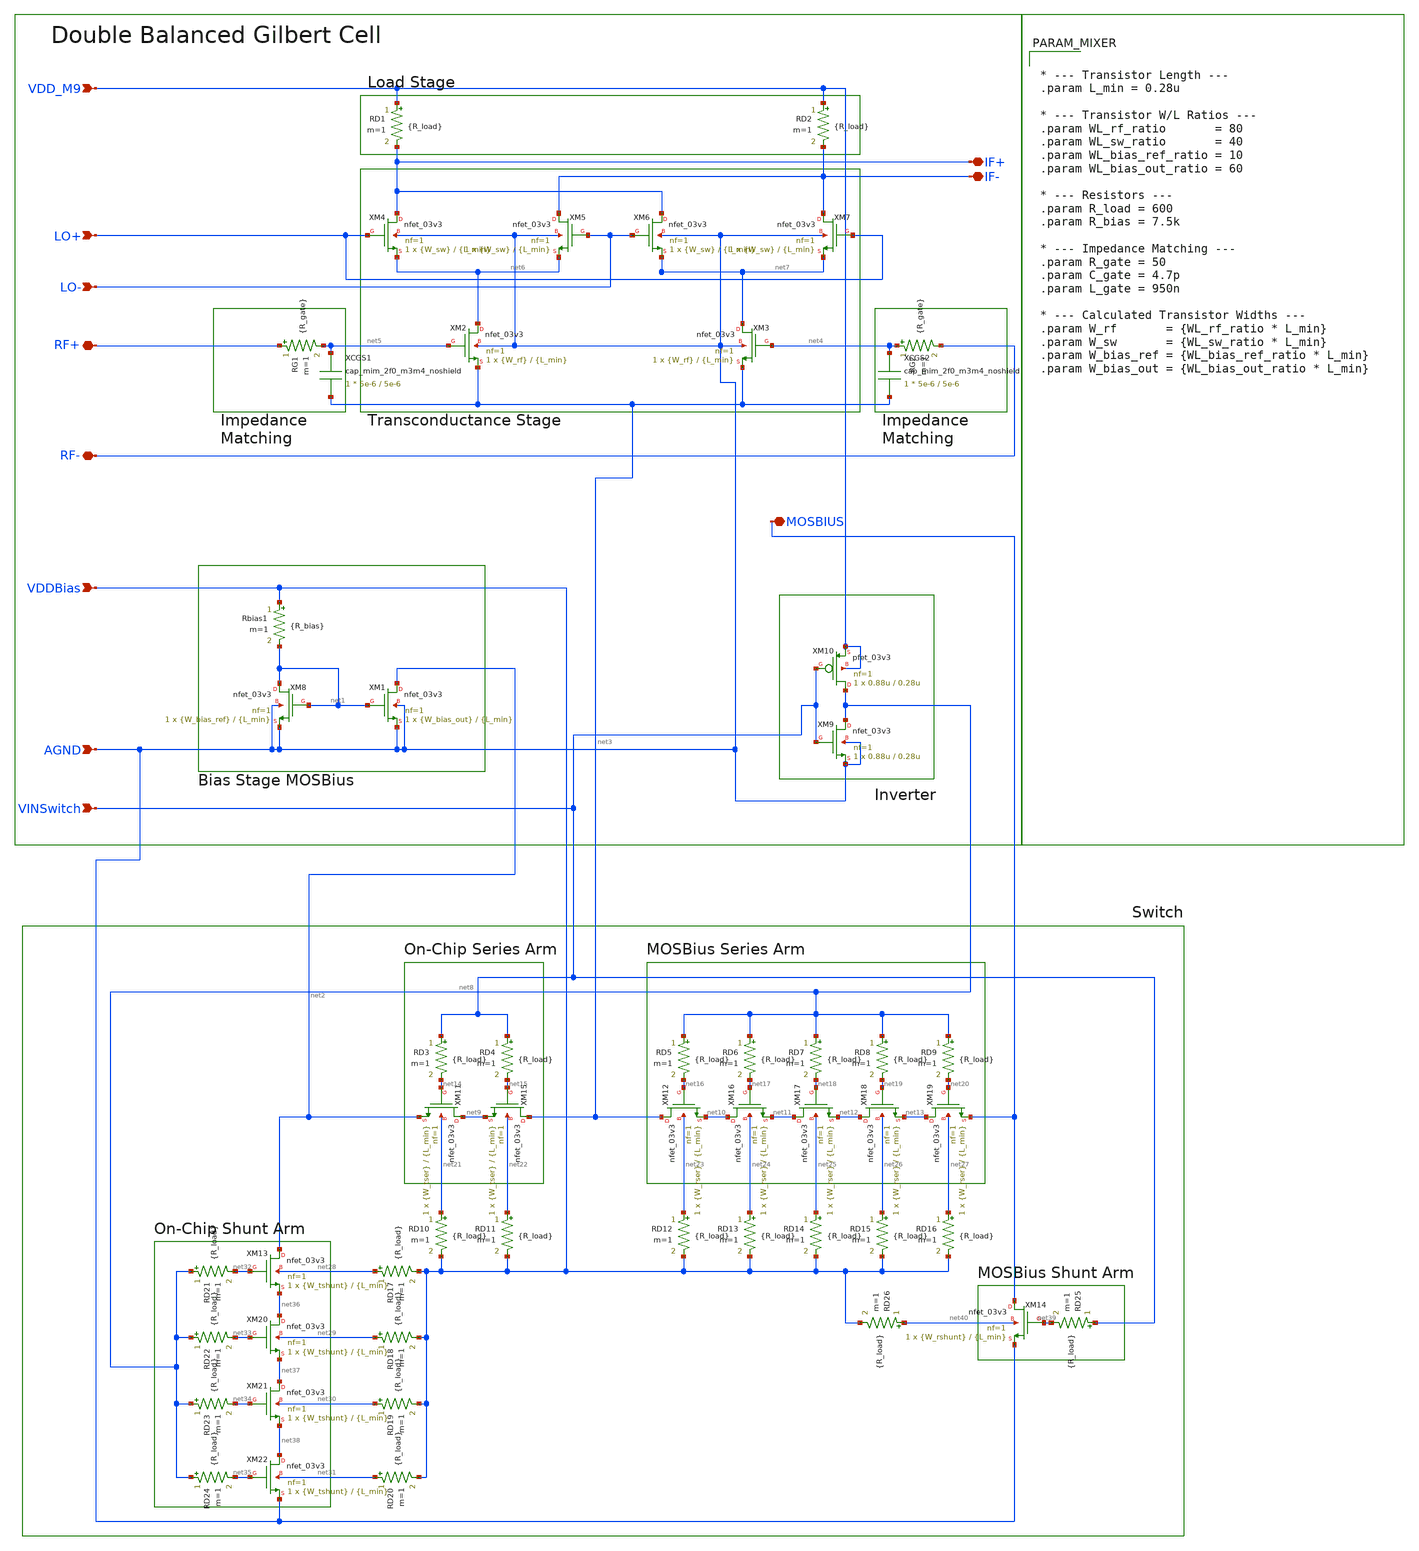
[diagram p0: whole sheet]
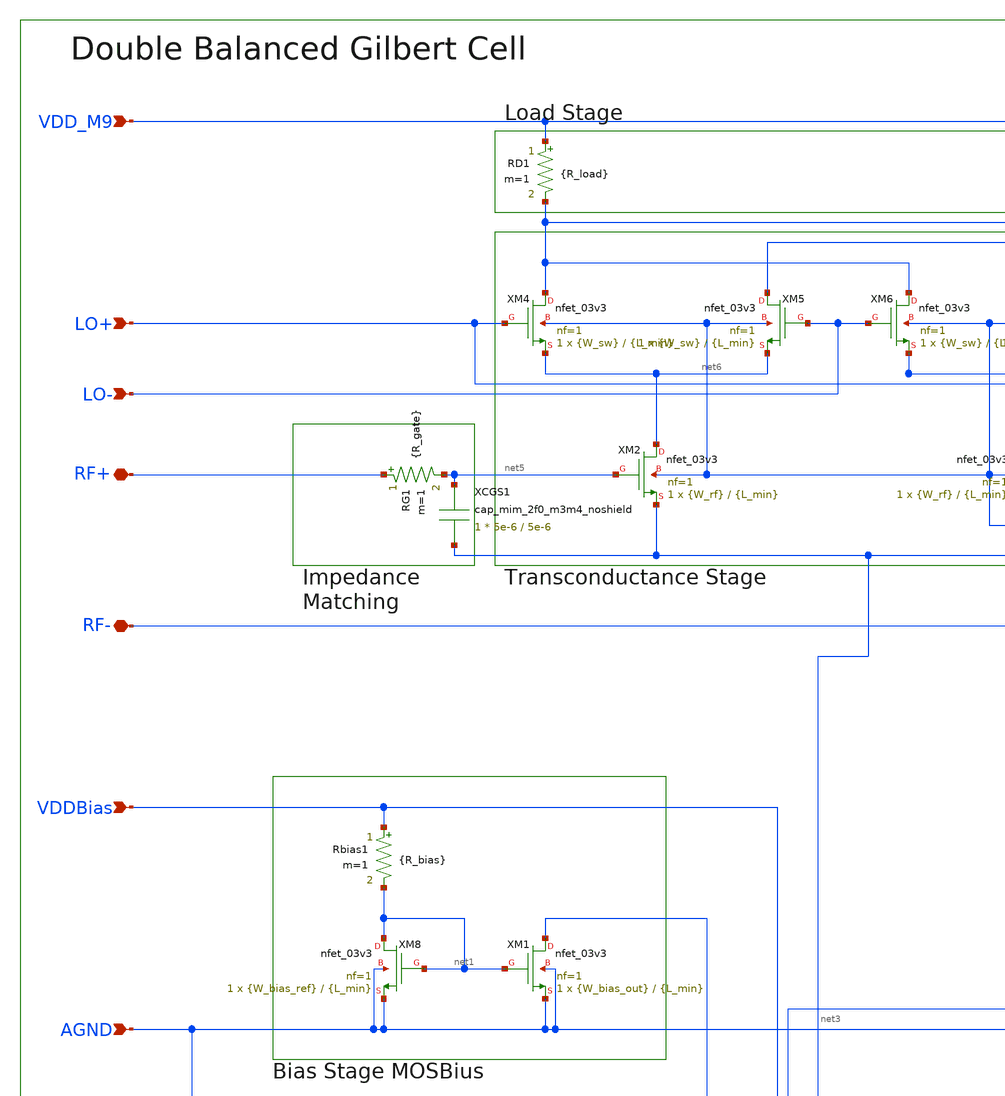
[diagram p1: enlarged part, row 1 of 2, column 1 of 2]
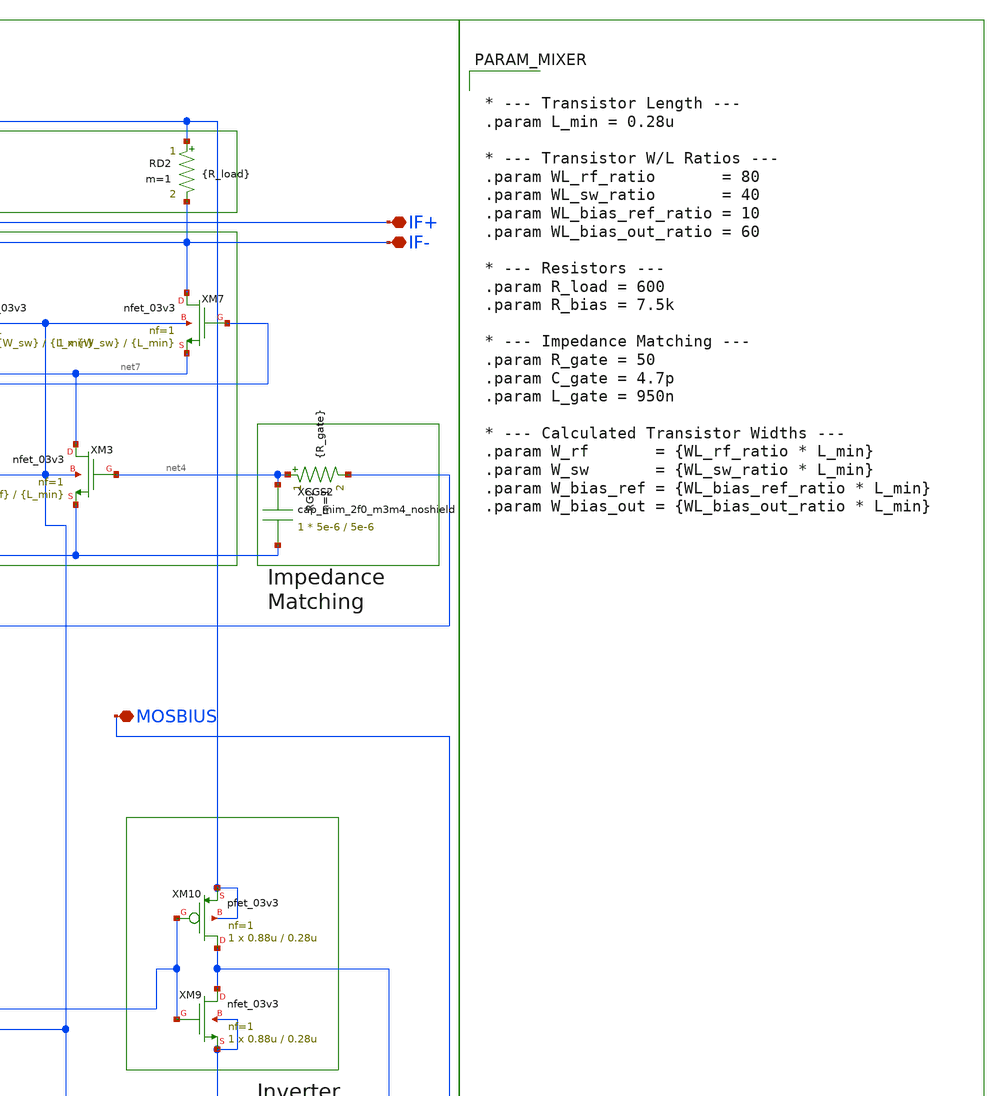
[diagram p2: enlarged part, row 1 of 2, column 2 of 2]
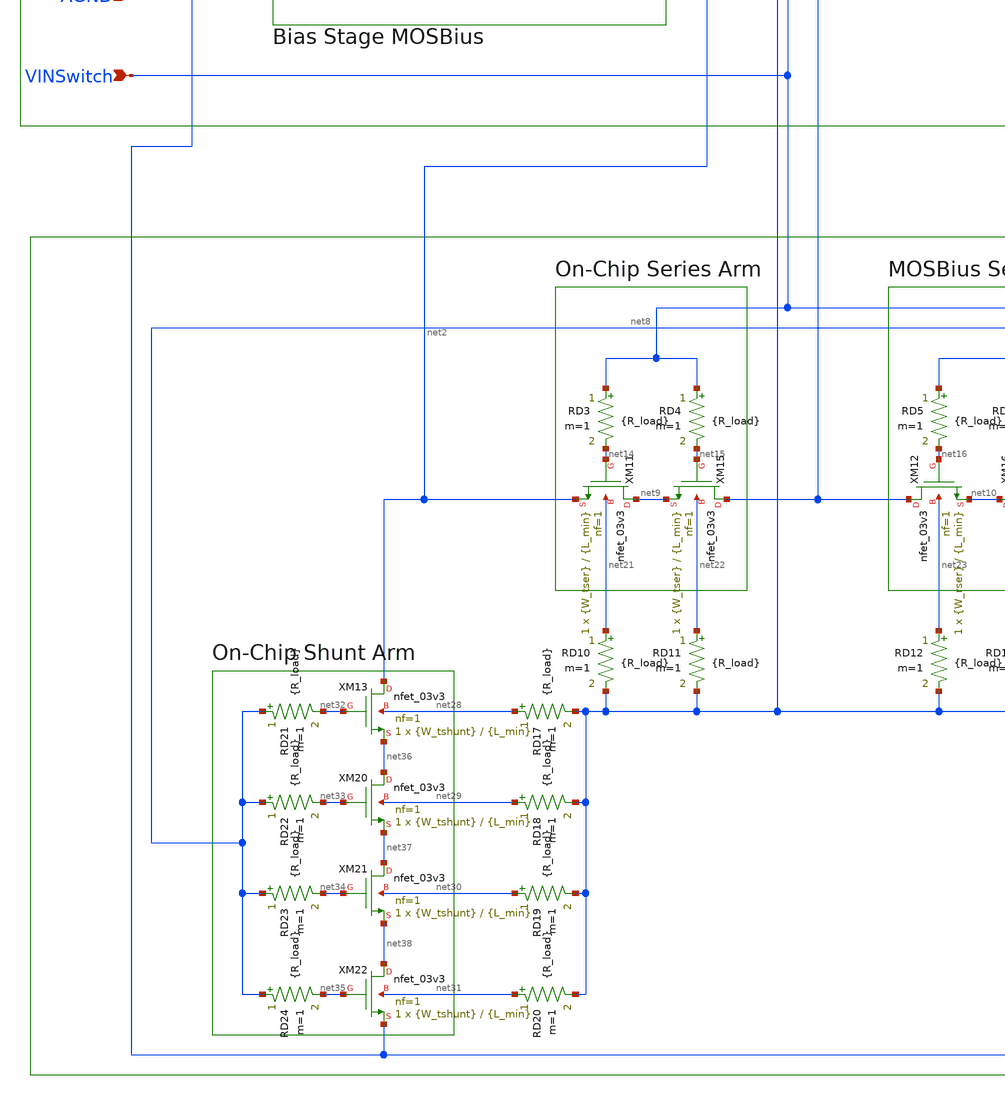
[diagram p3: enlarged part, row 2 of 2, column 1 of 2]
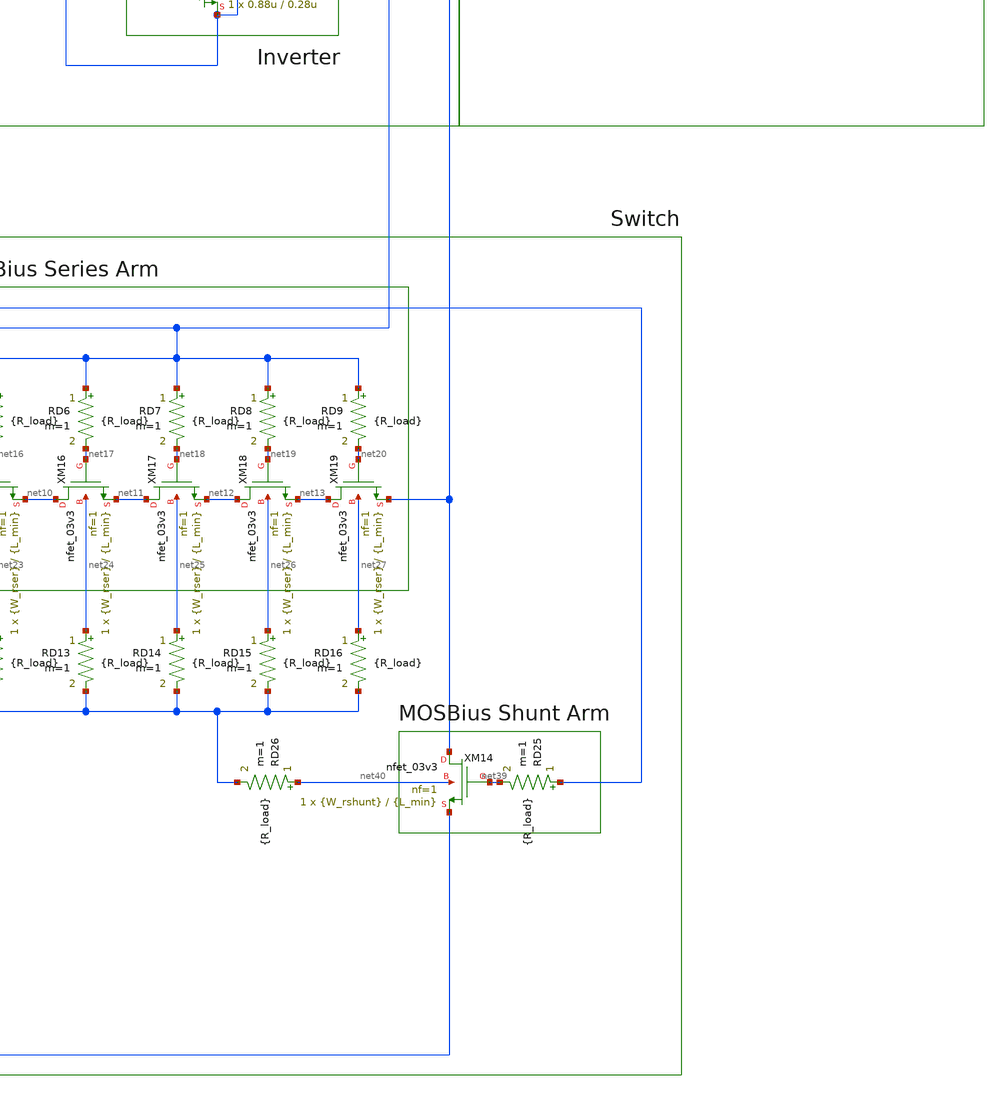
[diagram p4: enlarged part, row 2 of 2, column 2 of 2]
** sch_path: designs/libs/LVS/ReconfigMixer.sch
**.subckt ReconfigMixer AGND RF- IF+ VDD_M9 LO+ LO- IF- RF+ VDDBias MOSBIUS VINSwitch
*.ipin AGND
*.iopin RF-
*.iopin IF+
*.ipin VDD_M9
*.ipin LO+
*.ipin LO-
*.iopin IF-
*.iopin RF+
*.ipin VDDBias
*.iopin MOSBIUS
*.ipin VINSwitch
XM8 net1 net1 AGND AGND nfet_03v3 L={L_min} W={W_bias_ref} nf=1 ad='int((nf+1)/2) * W/nf * 0.18u' as='int((nf+2)/2) * W/nf * 0.18u'
+ pd='2*int((nf+1)/2) * (W/nf + 0.18u)' ps='2*int((nf+2)/2) * (W/nf + 0.18u)' nrd='0.18u / W' nrs='0.18u / W'
+ sa=0 sb=0 sd=0 m=1
XM1 net2 net1 AGND AGND nfet_03v3 L={L_min} W={W_bias_out} nf=1 ad='int((nf+1)/2) * W/nf * 0.18u' as='int((nf+2)/2) * W/nf * 0.18u'
+ pd='2*int((nf+1)/2) * (W/nf + 0.18u)' ps='2*int((nf+2)/2) * (W/nf + 0.18u)' nrd='0.18u / W' nrs='0.18u / W'
+ sa=0 sb=0 sd=0 m=1
XM3 net7 net4 net3 AGND nfet_03v3 L={L_min} W={W_rf} nf=1 ad='int((nf+1)/2) * W/nf * 0.18u' as='int((nf+2)/2) * W/nf * 0.18u'
+ pd='2*int((nf+1)/2) * (W/nf + 0.18u)' ps='2*int((nf+2)/2) * (W/nf + 0.18u)' nrd='0.18u / W' nrs='0.18u / W'
+ sa=0 sb=0 sd=0 m=1
XM2 net6 net5 net3 AGND nfet_03v3 L={L_min} W={W_rf} nf=1 ad='int((nf+1)/2) * W/nf * 0.18u' as='int((nf+2)/2) * W/nf * 0.18u'
+ pd='2*int((nf+1)/2) * (W/nf + 0.18u)' ps='2*int((nf+2)/2) * (W/nf + 0.18u)' nrd='0.18u / W' nrs='0.18u / W'
+ sa=0 sb=0 sd=0 m=1
XM7 IF- LO+ net7 AGND nfet_03v3 L={L_min} W={W_sw} nf=1 ad='int((nf+1)/2) * W/nf * 0.18u' as='int((nf+2)/2) * W/nf * 0.18u'
+ pd='2*int((nf+1)/2) * (W/nf + 0.18u)' ps='2*int((nf+2)/2) * (W/nf + 0.18u)' nrd='0.18u / W' nrs='0.18u / W'
+ sa=0 sb=0 sd=0 m=1
XM6 IF+ LO- net7 AGND nfet_03v3 L={L_min} W={W_sw} nf=1 ad='int((nf+1)/2) * W/nf * 0.18u' as='int((nf+2)/2) * W/nf * 0.18u'
+ pd='2*int((nf+1)/2) * (W/nf + 0.18u)' ps='2*int((nf+2)/2) * (W/nf + 0.18u)' nrd='0.18u / W' nrs='0.18u / W'
+ sa=0 sb=0 sd=0 m=1
XM5 IF- LO- net6 AGND nfet_03v3 L={L_min} W={W_sw} nf=1 ad='int((nf+1)/2) * W/nf * 0.18u' as='int((nf+2)/2) * W/nf * 0.18u'
+ pd='2*int((nf+1)/2) * (W/nf + 0.18u)' ps='2*int((nf+2)/2) * (W/nf + 0.18u)' nrd='0.18u / W' nrs='0.18u / W'
+ sa=0 sb=0 sd=0 m=1
XM4 IF+ LO+ net6 AGND nfet_03v3 L={L_min} W={W_sw} nf=1 ad='int((nf+1)/2) * W/nf * 0.18u' as='int((nf+2)/2) * W/nf * 0.18u'
+ pd='2*int((nf+1)/2) * (W/nf + 0.18u)' ps='2*int((nf+2)/2) * (W/nf + 0.18u)' nrd='0.18u / W' nrs='0.18u / W'
+ sa=0 sb=0 sd=0 m=1
RD1 VDD_M9 IF+ {R_load} m=1
RD2 VDD_M9 IF- {R_load} m=1
RG1 RF+ net5 {R_gate} m=1
RG2 net4 RF- {R_gate} m=1
Rbias1 VDDBias net1 {R_bias} m=1
XCGS2 net4 net3 cap_mim_2f0_m3m4_noshield c_width=5e-6 c_length=5e-6 m=1
XCGS1 net5 net3 cap_mim_2f0_m3m4_noshield c_width=5e-6 c_length=5e-6 m=1
XM9 net8 VINSwitch AGND AGND nfet_03v3 L=0.28u W=0.88u nf=1 ad='int((nf+1)/2) * W/nf * 0.18u' as='int((nf+2)/2) * W/nf * 0.18u'
+ pd='2*int((nf+1)/2) * (W/nf + 0.18u)' ps='2*int((nf+2)/2) * (W/nf + 0.18u)' nrd='0.18u / W' nrs='0.18u / W'
+ sa=0 sb=0 sd=0 m=1
XM10 net8 VINSwitch VDD_M9 VDD_M9 pfet_03v3 L=0.28u W=0.88u nf=1 ad='int((nf+1)/2) * W/nf * 0.18u' as='int((nf+2)/2) * W/nf * 0.18u'
+ pd='2*int((nf+1)/2) * (W/nf + 0.18u)' ps='2*int((nf+2)/2) * (W/nf + 0.18u)' nrd='0.18u / W' nrs='0.18u / W'
+ sa=0 sb=0 sd=0 m=1
XM11 net9 net14 net2 net21 nfet_03v3 L={L_min} W={W_tser} nf=1 ad='int((nf+1)/2) * W/nf * 0.18u' as='int((nf+2)/2) * W/nf * 0.18u'
+ pd='2*int((nf+1)/2) * (W/nf + 0.18u)' ps='2*int((nf+2)/2) * (W/nf + 0.18u)' nrd='0.18u / W' nrs='0.18u / W'
+ sa=0 sb=0 sd=0 m=1
XM12 net3 net16 net10 net23 nfet_03v3 L={L_min} W={W_rser} nf=1 ad='int((nf+1)/2) * W/nf * 0.18u' as='int((nf+2)/2) * W/nf * 0.18u'
+ pd='2*int((nf+1)/2) * (W/nf + 0.18u)' ps='2*int((nf+2)/2) * (W/nf + 0.18u)' nrd='0.18u / W' nrs='0.18u / W'
+ sa=0 sb=0 sd=0 m=1
XM13 net2 net32 net36 net28 nfet_03v3 L={L_min} W={W_tshunt} nf=1 ad='int((nf+1)/2) * W/nf * 0.18u' as='int((nf+2)/2) * W/nf * 0.18u'
+ pd='2*int((nf+1)/2) * (W/nf + 0.18u)' ps='2*int((nf+2)/2) * (W/nf + 0.18u)' nrd='0.18u / W' nrs='0.18u / W'
+ sa=0 sb=0 sd=0 m=1
XM14 MOSBIUS net39 AGND net40 nfet_03v3 L={L_min} W={W_rshunt} nf=1 ad='int((nf+1)/2) * W/nf * 0.18u'
+ as='int((nf+2)/2) * W/nf * 0.18u' pd='2*int((nf+1)/2) * (W/nf + 0.18u)' ps='2*int((nf+2)/2) * (W/nf + 0.18u)'
+ nrd='0.18u / W' nrs='0.18u / W' sa=0 sb=0 sd=0 m=1
XM15 net3 net15 net9 net22 nfet_03v3 L={L_min} W={W_tser} nf=1 ad='int((nf+1)/2) * W/nf * 0.18u' as='int((nf+2)/2) * W/nf * 0.18u'
+ pd='2*int((nf+1)/2) * (W/nf + 0.18u)' ps='2*int((nf+2)/2) * (W/nf + 0.18u)' nrd='0.18u / W' nrs='0.18u / W'
+ sa=0 sb=0 sd=0 m=1
RD3 VINSwitch net14 {R_load} m=1
RD4 VINSwitch net15 {R_load} m=1
RD5 net8 net16 {R_load} m=1
RD6 net8 net17 {R_load} m=1
RD7 net8 net18 {R_load} m=1
RD8 net8 net19 {R_load} m=1
RD9 net8 net20 {R_load} m=1
RD10 net21 VDDBias {R_load} m=1
RD11 net22 VDDBias {R_load} m=1
RD12 net23 VDDBias {R_load} m=1
RD13 net24 VDDBias {R_load} m=1
RD14 net25 VDDBias {R_load} m=1
RD15 net26 VDDBias {R_load} m=1
RD16 net27 VDDBias {R_load} m=1
RD17 net28 VDDBias {R_load} m=1
RD18 net29 VDDBias {R_load} m=1
RD19 net30 VDDBias {R_load} m=1
RD20 net31 VDDBias {R_load} m=1
RD21 net8 net32 {R_load} m=1
RD22 net8 net33 {R_load} m=1
RD23 net8 net34 {R_load} m=1
RD24 net8 net35 {R_load} m=1
XM16 net10 net17 net11 net24 nfet_03v3 L={L_min} W={W_rser} nf=1 ad='int((nf+1)/2) * W/nf * 0.18u' as='int((nf+2)/2) * W/nf * 0.18u'
+ pd='2*int((nf+1)/2) * (W/nf + 0.18u)' ps='2*int((nf+2)/2) * (W/nf + 0.18u)' nrd='0.18u / W' nrs='0.18u / W'
+ sa=0 sb=0 sd=0 m=1
XM17 net11 net18 net12 net25 nfet_03v3 L={L_min} W={W_rser} nf=1 ad='int((nf+1)/2) * W/nf * 0.18u' as='int((nf+2)/2) * W/nf * 0.18u'
+ pd='2*int((nf+1)/2) * (W/nf + 0.18u)' ps='2*int((nf+2)/2) * (W/nf + 0.18u)' nrd='0.18u / W' nrs='0.18u / W'
+ sa=0 sb=0 sd=0 m=1
XM18 net12 net19 net13 net26 nfet_03v3 L={L_min} W={W_rser} nf=1 ad='int((nf+1)/2) * W/nf * 0.18u' as='int((nf+2)/2) * W/nf * 0.18u'
+ pd='2*int((nf+1)/2) * (W/nf + 0.18u)' ps='2*int((nf+2)/2) * (W/nf + 0.18u)' nrd='0.18u / W' nrs='0.18u / W'
+ sa=0 sb=0 sd=0 m=1
XM19 net13 net20 MOSBIUS net27 nfet_03v3 L={L_min} W={W_rser} nf=1 ad='int((nf+1)/2) * W/nf * 0.18u'
+ as='int((nf+2)/2) * W/nf * 0.18u' pd='2*int((nf+1)/2) * (W/nf + 0.18u)' ps='2*int((nf+2)/2) * (W/nf + 0.18u)'
+ nrd='0.18u / W' nrs='0.18u / W' sa=0 sb=0 sd=0 m=1
RD25 VINSwitch net39 {R_load} m=1
XM20 net36 net33 net37 net29 nfet_03v3 L={L_min} W={W_tshunt} nf=1 ad='int((nf+1)/2) * W/nf * 0.18u'
+ as='int((nf+2)/2) * W/nf * 0.18u' pd='2*int((nf+1)/2) * (W/nf + 0.18u)' ps='2*int((nf+2)/2) * (W/nf + 0.18u)'
+ nrd='0.18u / W' nrs='0.18u / W' sa=0 sb=0 sd=0 m=1
XM21 net37 net34 net38 net30 nfet_03v3 L={L_min} W={W_tshunt} nf=1 ad='int((nf+1)/2) * W/nf * 0.18u'
+ as='int((nf+2)/2) * W/nf * 0.18u' pd='2*int((nf+1)/2) * (W/nf + 0.18u)' ps='2*int((nf+2)/2) * (W/nf + 0.18u)'
+ nrd='0.18u / W' nrs='0.18u / W' sa=0 sb=0 sd=0 m=1
XM22 net38 net35 AGND net31 nfet_03v3 L={L_min} W={W_tshunt} nf=1 ad='int((nf+1)/2) * W/nf * 0.18u' as='int((nf+2)/2) * W/nf * 0.18u'
+ pd='2*int((nf+1)/2) * (W/nf + 0.18u)' ps='2*int((nf+2)/2) * (W/nf + 0.18u)' nrd='0.18u / W' nrs='0.18u / W'
+ sa=0 sb=0 sd=0 m=1
RD26 net40 VDDBias {R_load} m=1
**** begin user architecture code


* --- Transistor Length ---
.param L_min = 0.28u

* --- Transistor W/L Ratios ---
.param WL_rf_ratio       = 80
.param WL_sw_ratio       = 40
.param WL_bias_ref_ratio = 10
.param WL_bias_out_ratio = 60

* --- Resistors ---
.param R_load = 600
.param R_bias = 7.5k

* --- Impedance Matching ---
.param R_gate = 50
.param C_gate = 4.7p
.param L_gate = 950n

* --- Calculated Transistor Widths ---
.param W_rf       = {WL_rf_ratio * L_min}
.param W_sw       = {WL_sw_ratio * L_min}
.param W_bias_ref = {WL_bias_ref_ratio * L_min}
.param W_bias_out = {WL_bias_out_ratio * L_min}


**** end user architecture code
**.ends
.end
